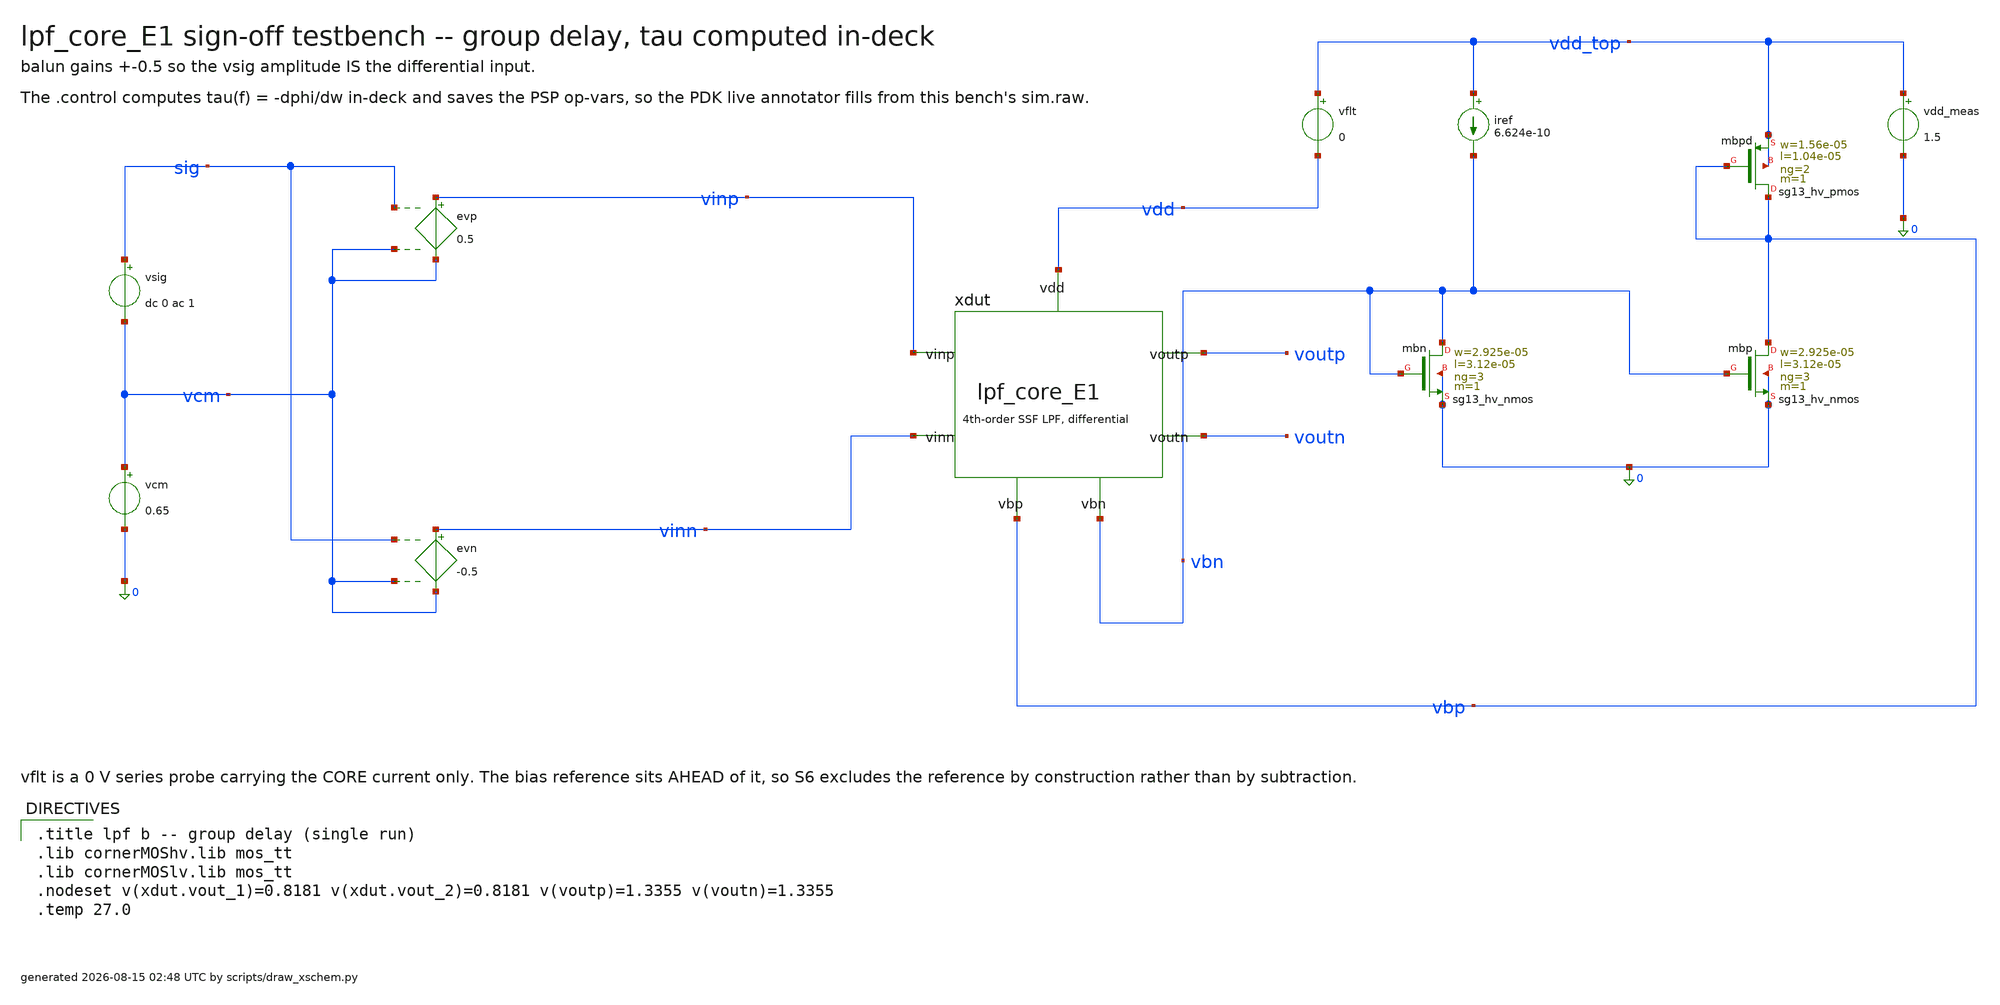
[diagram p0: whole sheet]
** sch_path: signoff/pre-pvt/E1-prev/lpf_tb_E1_gd.sch
**.subckt lpf_tb_E1_gd
vsig sig vcm dc 0 ac 1
vcm vcm 0 0.65
evp vinp vcm sig vcm 0.5
evn vinn vcm sig vcm -0.5
xdut vinp vinn voutp voutn vbn vbp vdd lpf_core_E1
vflt vdd_top vdd 0
vdd_meas vdd_top 0 1.5
iref vdd_top vbn 6.624e-10
Xmbn vbn vbn 0 0 sg13_hv_nmos w=2.925e-05 l=3.12e-05 ng=3 m=1 mm_ok=1
Xmbp vbp vbn 0 0 sg13_hv_nmos w=2.925e-05 l=3.12e-05 ng=3 m=1 mm_ok=1
Xmbpd vbp vbp vdd_top vdd_top sg13_hv_pmos w=1.56e-05 l=1.04e-05 ng=2 m=1 mm_ok=1
**** begin user architecture code

.title lpf b -- group delay (single run)
.lib cornerMOShv.lib mos_tt
.lib cornerMOSlv.lib mos_tt
.nodeset v(xdut.vout_1)=0.8181 v(xdut.vout_2)=0.8181 v(voutp)=1.3355 v(voutn)=1.3355
.temp 27.0


.control
set filetype=binary
set appendwrite
save all @n.xdut.xm2.nsg13_lv_pmos[ids] @n.xdut.xm2.nsg13_lv_pmos[gm] @n.xdut.xm2.nsg13_lv_pmos[gds]
+ @n.xdut.xm2.nsg13_lv_pmos[gmb] @n.xdut.xm2.nsg13_lv_pmos[vgs] @n.xdut.xm2.nsg13_lv_pmos[vds] @n.xdut.xm2.nsg13_lv_pmos[vth]
+ @n.xdut.xm2.nsg13_lv_pmos[vdss] @n.xdut.xm2.nsg13_lv_pmos[cgg] @n.xdut.xm5.nsg13_lv_pmos[ids] @n.xdut.xm5.nsg13_lv_pmos[gm]
+ @n.xdut.xm5.nsg13_lv_pmos[gds] @n.xdut.xm5.nsg13_lv_pmos[gmb] @n.xdut.xm5.nsg13_lv_pmos[vgs] @n.xdut.xm5.nsg13_lv_pmos[vds]
+ @n.xdut.xm5.nsg13_lv_pmos[vth] @n.xdut.xm5.nsg13_lv_pmos[vdss] @n.xdut.xm5.nsg13_lv_pmos[cgg] @n.xdut.xm4.nsg13_hv_nmos[ids]
+ @n.xdut.xm4.nsg13_hv_nmos[gm] @n.xdut.xm4.nsg13_hv_nmos[gds] @n.xdut.xm4.nsg13_hv_nmos[gmb] @n.xdut.xm4.nsg13_hv_nmos[vgs]
+ @n.xdut.xm4.nsg13_hv_nmos[vds] @n.xdut.xm4.nsg13_hv_nmos[vth] @n.xdut.xm4.nsg13_hv_nmos[vdss] @n.xdut.xm4.nsg13_hv_nmos[cgg]
+ @n.xdut.xm8.nsg13_hv_nmos[ids] @n.xdut.xm8.nsg13_hv_nmos[gm] @n.xdut.xm8.nsg13_hv_nmos[gds] @n.xdut.xm8.nsg13_hv_nmos[gmb]
+ @n.xdut.xm8.nsg13_hv_nmos[vgs] @n.xdut.xm8.nsg13_hv_nmos[vds] @n.xdut.xm8.nsg13_hv_nmos[vth] @n.xdut.xm8.nsg13_hv_nmos[vdss]
+ @n.xdut.xm8.nsg13_hv_nmos[cgg] @n.xdut.xm9.nsg13_hv_nmos[ids] @n.xdut.xm9.nsg13_hv_nmos[gm] @n.xdut.xm9.nsg13_hv_nmos[gds]
+ @n.xdut.xm9.nsg13_hv_nmos[gmb] @n.xdut.xm9.nsg13_hv_nmos[vgs] @n.xdut.xm9.nsg13_hv_nmos[vds] @n.xdut.xm9.nsg13_hv_nmos[vth]
+ @n.xdut.xm9.nsg13_hv_nmos[vdss] @n.xdut.xm9.nsg13_hv_nmos[cgg] @n.xdut.xm10.nsg13_hv_nmos[ids] @n.xdut.xm10.nsg13_hv_nmos[gm]
+ @n.xdut.xm10.nsg13_hv_nmos[gds] @n.xdut.xm10.nsg13_hv_nmos[gmb] @n.xdut.xm10.nsg13_hv_nmos[vgs] @n.xdut.xm10.nsg13_hv_nmos[vds]
+ @n.xdut.xm10.nsg13_hv_nmos[vth] @n.xdut.xm10.nsg13_hv_nmos[vdss] @n.xdut.xm10.nsg13_hv_nmos[cgg] @n.xdut.xmst.nsg13_hv_pmos[ids]
+ @n.xdut.xmst.nsg13_hv_pmos[gm] @n.xdut.xmst.nsg13_hv_pmos[gds] @n.xdut.xmst.nsg13_hv_pmos[gmb] @n.xdut.xmst.nsg13_hv_pmos[vgs]
+ @n.xdut.xmst.nsg13_hv_pmos[vds] @n.xdut.xmst.nsg13_hv_pmos[vth] @n.xdut.xmst.nsg13_hv_pmos[vdss] @n.xdut.xmst.nsg13_hv_pmos[cgg]
+ @n.xdut.xmstn.nsg13_hv_pmos[ids] @n.xdut.xmstn.nsg13_hv_pmos[gm] @n.xdut.xmstn.nsg13_hv_pmos[gds] @n.xdut.xmstn.nsg13_hv_pmos[gmb]
+ @n.xdut.xmstn.nsg13_hv_pmos[vgs] @n.xdut.xmstn.nsg13_hv_pmos[vds] @n.xdut.xmstn.nsg13_hv_pmos[vth] @n.xdut.xmstn.nsg13_hv_pmos[vdss]
+ @n.xdut.xmstn.nsg13_hv_pmos[cgg] @n.xdut.xm0.nsg13_hv_pmos[ids] @n.xdut.xm0.nsg13_hv_pmos[gm] @n.xdut.xm0.nsg13_hv_pmos[gds]
+ @n.xdut.xm0.nsg13_hv_pmos[gmb] @n.xdut.xm0.nsg13_hv_pmos[vgs] @n.xdut.xm0.nsg13_hv_pmos[vds] @n.xdut.xm0.nsg13_hv_pmos[vth]
+ @n.xdut.xm0.nsg13_hv_pmos[vdss] @n.xdut.xm0.nsg13_hv_pmos[cgg] @n.xdut.xm1.nsg13_hv_pmos[ids] @n.xdut.xm1.nsg13_hv_pmos[gm]
+ @n.xdut.xm1.nsg13_hv_pmos[gds] @n.xdut.xm1.nsg13_hv_pmos[gmb] @n.xdut.xm1.nsg13_hv_pmos[vgs] @n.xdut.xm1.nsg13_hv_pmos[vds]
+ @n.xdut.xm1.nsg13_hv_pmos[vth] @n.xdut.xm1.nsg13_hv_pmos[vdss] @n.xdut.xm1.nsg13_hv_pmos[cgg] @n.xdut.xm14.nsg13_lv_pmos[ids]
+ @n.xdut.xm14.nsg13_lv_pmos[gm] @n.xdut.xm14.nsg13_lv_pmos[gds] @n.xdut.xm14.nsg13_lv_pmos[gmb] @n.xdut.xm14.nsg13_lv_pmos[vgs]
+ @n.xdut.xm14.nsg13_lv_pmos[vds] @n.xdut.xm14.nsg13_lv_pmos[vth] @n.xdut.xm14.nsg13_lv_pmos[vdss] @n.xdut.xm14.nsg13_lv_pmos[cgg]
+ @n.xdut.xm15.nsg13_lv_pmos[ids] @n.xdut.xm15.nsg13_lv_pmos[gm] @n.xdut.xm15.nsg13_lv_pmos[gds] @n.xdut.xm15.nsg13_lv_pmos[gmb]
+ @n.xdut.xm15.nsg13_lv_pmos[vgs] @n.xdut.xm15.nsg13_lv_pmos[vds] @n.xdut.xm15.nsg13_lv_pmos[vth] @n.xdut.xm15.nsg13_lv_pmos[vdss]
+ @n.xdut.xm15.nsg13_lv_pmos[cgg]
op
write sim.raw
ac dec 50 0.1 1000
let hdiff = v(voutp) - v(voutn)
let hdb = db(mag(hdiff))
let dc_db = hdb[0]
let ph = cph(hdiff)
let gd = -deriv(ph) / (2 * pi)
let gd_dc_ms = gd[0] * 1e3
let gd_max_ms = vecmax(gd) * 1e3
let hrel = hdb - dc_db
meas ac fc_hz when hrel = -3 fall = 1
print dc_db gd_dc_ms gd_max_ms
write sim.raw hdiff ph gd frequency
.endc

**** end user architecture code
**.ends

* expanding   symbol:  lpf_core_E1.sym # of pins=7
** sym_path: signoff/E1-prev/lpf_core_E1.sym
** sch_path: signoff/E1-prev/lpf_core_E1.sch
.subckt lpf_core_E1 vinp vinn voutp voutn vbn vbp vdd
*.ipin vinp
*.ipin vinn
*.opin voutp
*.opin voutn
*.ipin vdd
*.ipin vbn
*.ipin vbp
Xm2 net2 vinp vout_1 vout_1 sg13_lv_pmos w=1.56e-05 l=1.04e-05 ng=1 m=1 mm_ok=1
Xm5 net3 vinn vout_2 vout_2 sg13_lv_pmos w=1.56e-05 l=1.04e-05 ng=1 m=1 mm_ok=1
Xm4 vout_1 net2 0 0 sg13_hv_nmos w=7.8e-06 l=5.2e-06 ng=1 m=1 mm_ok=1
Xm8 vout_2 net3 0 0 sg13_hv_nmos w=7.8e-06 l=5.2e-06 ng=1 m=1 mm_ok=1
Xm9 net2 vbn 0 0 sg13_hv_nmos w=2.925e-05 l=3.12e-05 ng=1 m=1 mm_ok=1
Xm10 net3 vbn 0 0 sg13_hv_nmos w=2.925e-05 l=3.12e-05 ng=1 m=1 mm_ok=1
Xmst vout_1 vbn net4 net4 sg13_hv_pmos w=2.5896e-07 l=4.368e-05 ng=1 m=1 mm_ok=1
Xmstn vout_2 vbn net1 net1 sg13_hv_pmos w=2.5896e-07 l=4.368e-05 ng=1 m=1 mm_ok=1
Xm0 net4 vout_1 voutp voutp sg13_hv_pmos w=1.56e-05 l=1.04e-05 ng=1 m=1 mm_ok=1
Xm1 net1 vout_2 voutn voutn sg13_hv_pmos w=1.56e-05 l=1.04e-05 ng=1 m=1 mm_ok=1
Xm14 voutp net4 vdd vdd sg13_lv_pmos w=1.29324e-06 l=6.24e-05 ng=1 m=1 mm_ok=1
Xm15 voutn net1 vdd vdd sg13_lv_pmos w=1.29324e-06 l=6.24e-05 ng=1 m=1 mm_ok=1
c13 net2 vout_1 8.53159e-12 m=1
c17 net3 vout_2 8.53159e-12 m=1
c19 vout_2 vout_1 3.22133e-11 m=1
c1 voutp net4 8.17985e-11 m=1
c10 voutn net1 8.17985e-11 m=1
c12 voutn voutp 1.64735e-11 m=1
.ends

.end
